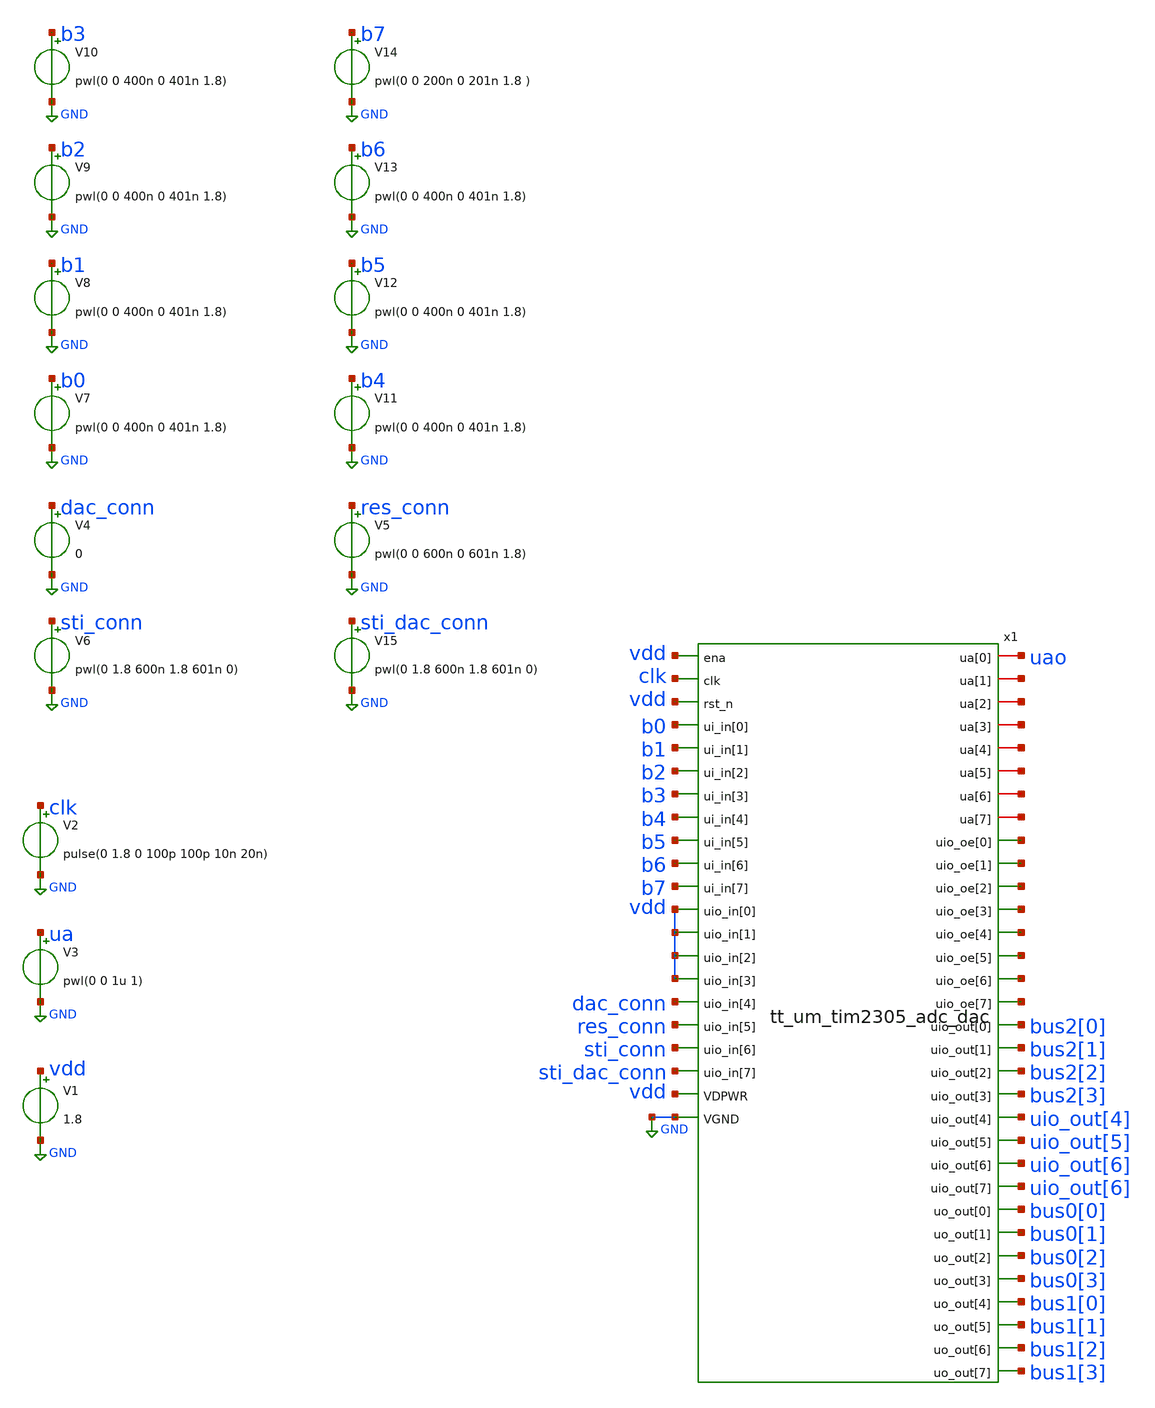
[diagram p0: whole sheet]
** sch_path: custom_gds/tt_um_tim2305_adc_dac/xschem/top_tb.sch
**.subckt top_tb
V1 vdd GND 1.8
V3 ua GND pwl(0 0 1u 1)
V2 clk GND pulse(0 1.8 0 100p 100p 10n 20n)
x1 clk vdd vdd uao net1 net2 net3 net4 net5 net6 net7 b0 b1 b2 b3 b4 b5 b6 b7 vdd vdd vdd vdd
+ dac_conn res_conn sti_conn sti_dac_conn net8 net9 net10 net11 net12 net13 net14 net15 bus2[0] bus2[1]
+ bus2[2] bus2[3] uio_out[4] uio_out[5] uio_out[6] uio_out[6] bus0[0] bus0[1] bus0[2] bus0[3] bus1[0] bus1[1]
+ bus1[2] bus1[3] vdd GND tt_um_tim2305_adc_dac
V7 b0 GND pwl(0 0 400n 0 401n 1.8)
V8 b1 GND pwl(0 0 400n 0 401n 1.8)
V9 b2 GND pwl(0 0 400n 0 401n 1.8)
V10 b3 GND pwl(0 0 400n 0 401n 1.8)
V11 b4 GND pwl(0 0 400n 0 401n 1.8)
V12 b5 GND pwl(0 0 400n 0 401n 1.8)
V13 b6 GND pwl(0 0 400n 0 401n 1.8)
V14 b7 GND pwl(0 0 200n 0 201n 1.8 )
V4 dac_conn GND 0
V5 res_conn GND pwl(0 0 600n 0 601n 1.8)
V6 sti_conn GND pwl(0 1.8 600n 1.8 601n 0)
V15 sti_dac_conn GND pwl(0 1.8 600n 1.8 601n 0)
**** begin user architecture code


.tran 100p 800n
.save all
.lib /home/ttuser/pdk/sky130A/libs.tech/ngspice/sky130.lib.spice tt
.include /home/ttuser/Documents/github_project/adc_dac2/mag/tt_um_tim2305_adc_dac.spice


**** end user architecture code
**.ends
.GLOBAL GND
.end
